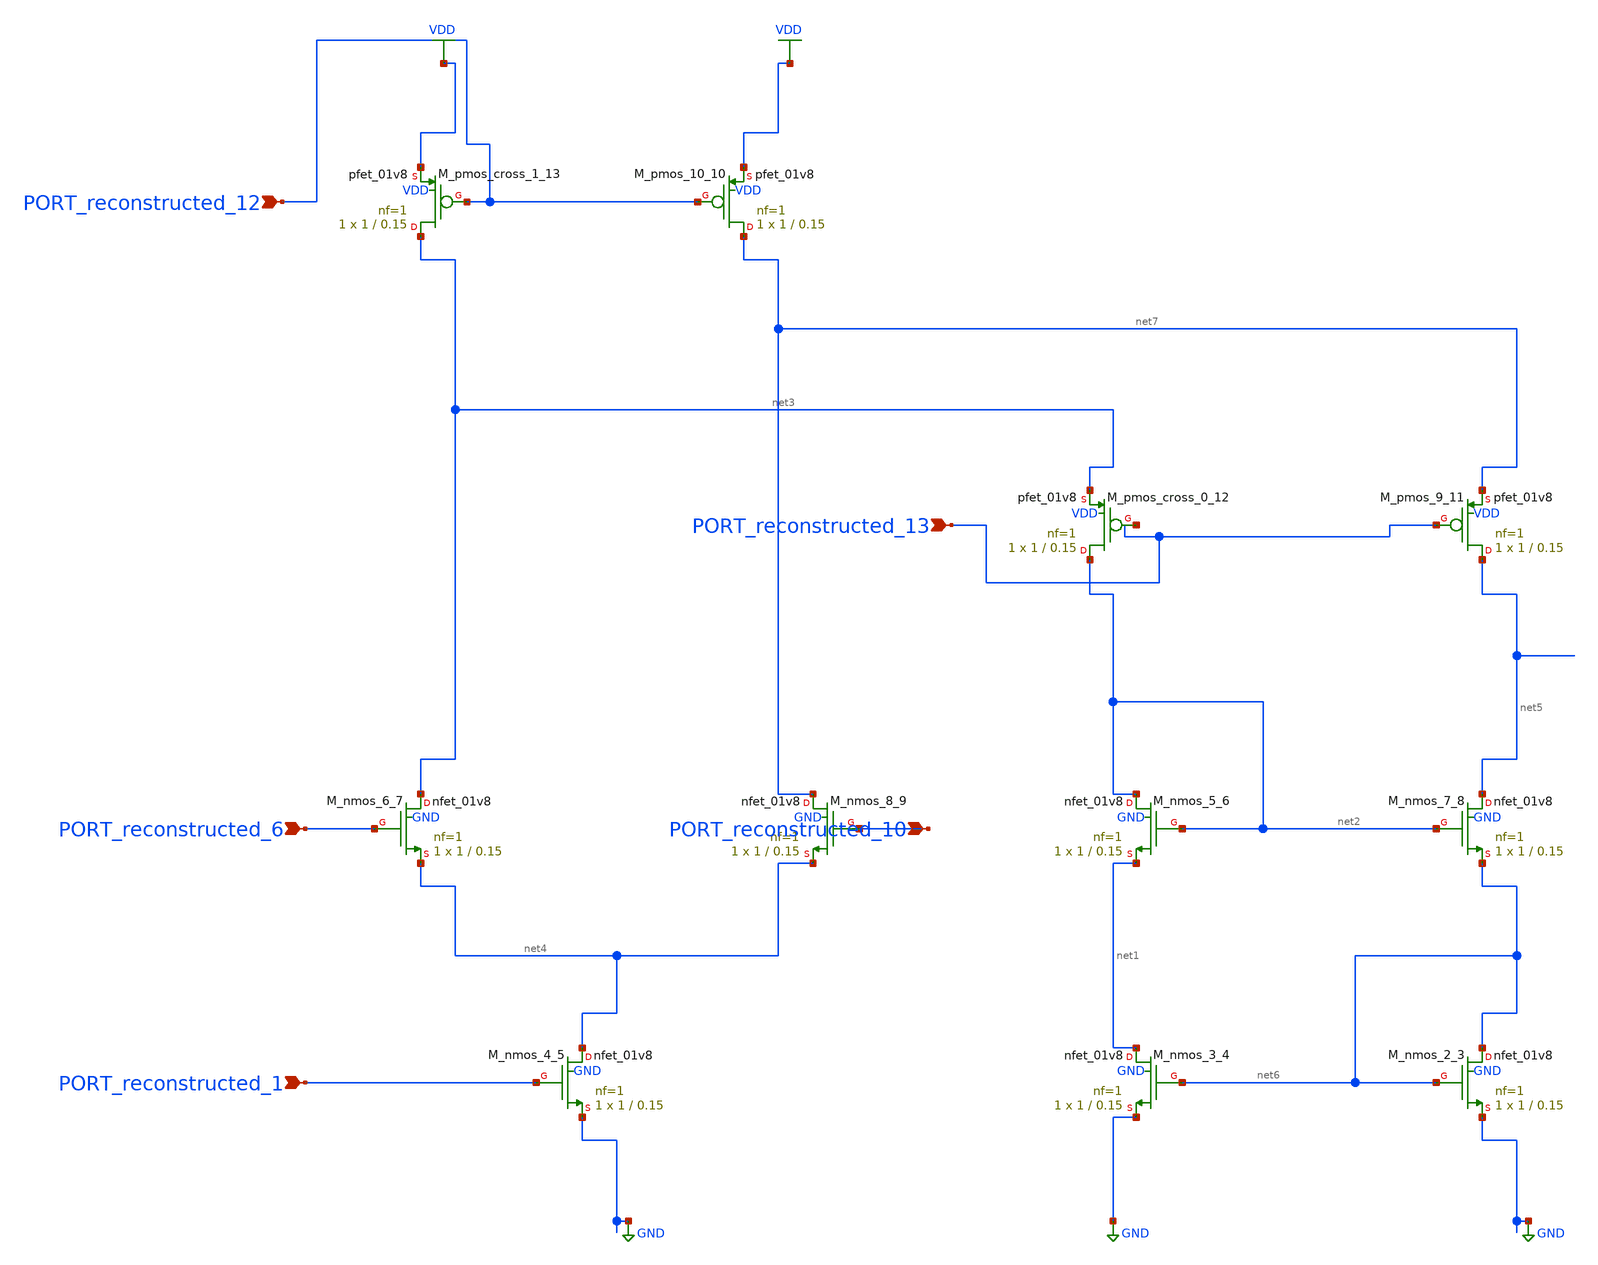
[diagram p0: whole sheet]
** sch_path: schematics/10_1007_BF02104746_101_001.sch
**.subckt 10_1007_BF02104746_101_001 PORT_reconstructed_6 PORT_reconstructed_12
*+ PORT_reconstructed_10 PORT_reconstructed_1 PORT_reconstructed_13
*.ipin PORT_reconstructed_6
*.ipin PORT_reconstructed_12
*.ipin PORT_reconstructed_10
*.ipin PORT_reconstructed_1
*.ipin PORT_reconstructed_13
XM_nmos_2_3 net6 net6 GND GND sky130_fd_pr__nfet_01v8 L=0.15 W=1 nf=1 ad='int((1 + 1)/2) * 1 / 1 * 0.29'
+ as='int((1 + 2)/2) * 1 / 1 * 0.29' pd='2*int((1 + 1)/2) * (1 / 1 + 0.29)' ps='2*int((1 + 2)/2) * (1 / 1 + 0.29)'
+ nrd='0.29 / 1 ' nrs='0.29 / 1 ' sa=0 sb=0 sd=0 mult=1 m=1
XM_nmos_3_4 net1 net6 GND GND sky130_fd_pr__nfet_01v8 L=0.15 W=1 nf=1 ad='int((1 + 1)/2) * 1 / 1 * 0.29'
+ as='int((1 + 2)/2) * 1 / 1 * 0.29' pd='2*int((1 + 1)/2) * (1 / 1 + 0.29)' ps='2*int((1 + 2)/2) * (1 / 1 + 0.29)'
+ nrd='0.29 / 1 ' nrs='0.29 / 1 ' sa=0 sb=0 sd=0 mult=1 m=1
XM_nmos_4_5 net4 PORT_reconstructed_1 GND GND sky130_fd_pr__nfet_01v8 L=0.15 W=1 nf=1 ad='int((1 + 1)/2) * 1 / 1 * 0.29'
+ as='int((1 + 2)/2) * 1 / 1 * 0.29' pd='2*int((1 + 1)/2) * (1 / 1 + 0.29)' ps='2*int((1 + 2)/2) * (1 / 1 + 0.29)'
+ nrd='0.29 / 1 ' nrs='0.29 / 1 ' sa=0 sb=0 sd=0 mult=1 m=1
XM_nmos_5_6 net2 net2 net1 GND sky130_fd_pr__nfet_01v8 L=0.15 W=1 nf=1 ad='int((1 + 1)/2) * 1 / 1 * 0.29'
+ as='int((1 + 2)/2) * 1 / 1 * 0.29' pd='2*int((1 + 1)/2) * (1 / 1 + 0.29)' ps='2*int((1 + 2)/2) * (1 / 1 + 0.29)'
+ nrd='0.29 / 1 ' nrs='0.29 / 1 ' sa=0 sb=0 sd=0 mult=1 m=1
XM_nmos_6_7 net3 PORT_reconstructed_6 net4 GND sky130_fd_pr__nfet_01v8 L=0.15 W=1 nf=1 ad='int((1 + 1)/2) * 1 / 1 * 0.29'
+ as='int((1 + 2)/2) * 1 / 1 * 0.29' pd='2*int((1 + 1)/2) * (1 / 1 + 0.29)' ps='2*int((1 + 2)/2) * (1 / 1 + 0.29)'
+ nrd='0.29 / 1 ' nrs='0.29 / 1 ' sa=0 sb=0 sd=0 mult=1 m=1
XM_nmos_7_8 net5 net2 net6 GND sky130_fd_pr__nfet_01v8 L=0.15 W=1 nf=1 ad='int((1 + 1)/2) * 1 / 1 * 0.29'
+ as='int((1 + 2)/2) * 1 / 1 * 0.29' pd='2*int((1 + 1)/2) * (1 / 1 + 0.29)' ps='2*int((1 + 2)/2) * (1 / 1 + 0.29)'
+ nrd='0.29 / 1 ' nrs='0.29 / 1 ' sa=0 sb=0 sd=0 mult=1 m=1
XM_nmos_8_9 net7 PORT_reconstructed_10 net4 GND sky130_fd_pr__nfet_01v8 L=0.15 W=1 nf=1 ad='int((1 + 1)/2) * 1 / 1 * 0.29'
+ as='int((1 + 2)/2) * 1 / 1 * 0.29' pd='2*int((1 + 1)/2) * (1 / 1 + 0.29)' ps='2*int((1 + 2)/2) * (1 / 1 + 0.29)'
+ nrd='0.29 / 1 ' nrs='0.29 / 1 ' sa=0 sb=0 sd=0 mult=1 m=1
XM_pmos_10_10 net7 PORT_reconstructed_12 VDD VDD sky130_fd_pr__pfet_01v8 L=0.15 W=1 nf=1 ad='int((1 + 1)/2) * 1 / 1 * 0.29'
+ as='int((1 + 2)/2) * 1 / 1 * 0.29' pd='2*int((1 + 1)/2) * (1 / 1 + 0.29)' ps='2*int((1 + 2)/2) * (1 / 1 + 0.29)'
+ nrd='0.29 / 1 ' nrs='0.29 / 1 ' sa=0 sb=0 sd=0 mult=1 m=1
XM_pmos_9_11 net5 PORT_reconstructed_13 net7 VDD sky130_fd_pr__pfet_01v8 L=0.15 W=1 nf=1 ad='int((1 + 1)/2) * 1 / 1 * 0.29'
+ as='int((1 + 2)/2) * 1 / 1 * 0.29' pd='2*int((1 + 1)/2) * (1 / 1 + 0.29)' ps='2*int((1 + 2)/2) * (1 / 1 + 0.29)'
+ nrd='0.29 / 1 ' nrs='0.29 / 1 ' sa=0 sb=0 sd=0 mult=1 m=1
XM_pmos_cross_0_12 net2 PORT_reconstructed_13 net3 VDD sky130_fd_pr__pfet_01v8 L=0.15 W=1 nf=1 ad='int((1 + 1)/2) * 1 / 1 * 0.29'
+ as='int((1 + 2)/2) * 1 / 1 * 0.29' pd='2*int((1 + 1)/2) * (1 / 1 + 0.29)' ps='2*int((1 + 2)/2) * (1 / 1 + 0.29)'
+ nrd='0.29 / 1 ' nrs='0.29 / 1 ' sa=0 sb=0 sd=0 mult=1 m=1
XM_pmos_cross_1_13 net3 PORT_reconstructed_12 VDD VDD sky130_fd_pr__pfet_01v8 L=0.15 W=1 nf=1 ad='int((1 + 1)/2) * 1 / 1 * 0.29'
+ as='int((1 + 2)/2) * 1 / 1 * 0.29' pd='2*int((1 + 1)/2) * (1 / 1 + 0.29)' ps='2*int((1 + 2)/2) * (1 / 1 + 0.29)'
+ nrd='0.29 / 1 ' nrs='0.29 / 1 ' sa=0 sb=0 sd=0 mult=1 m=1
**.ends
.GLOBAL GND
.GLOBAL VDD
.end
